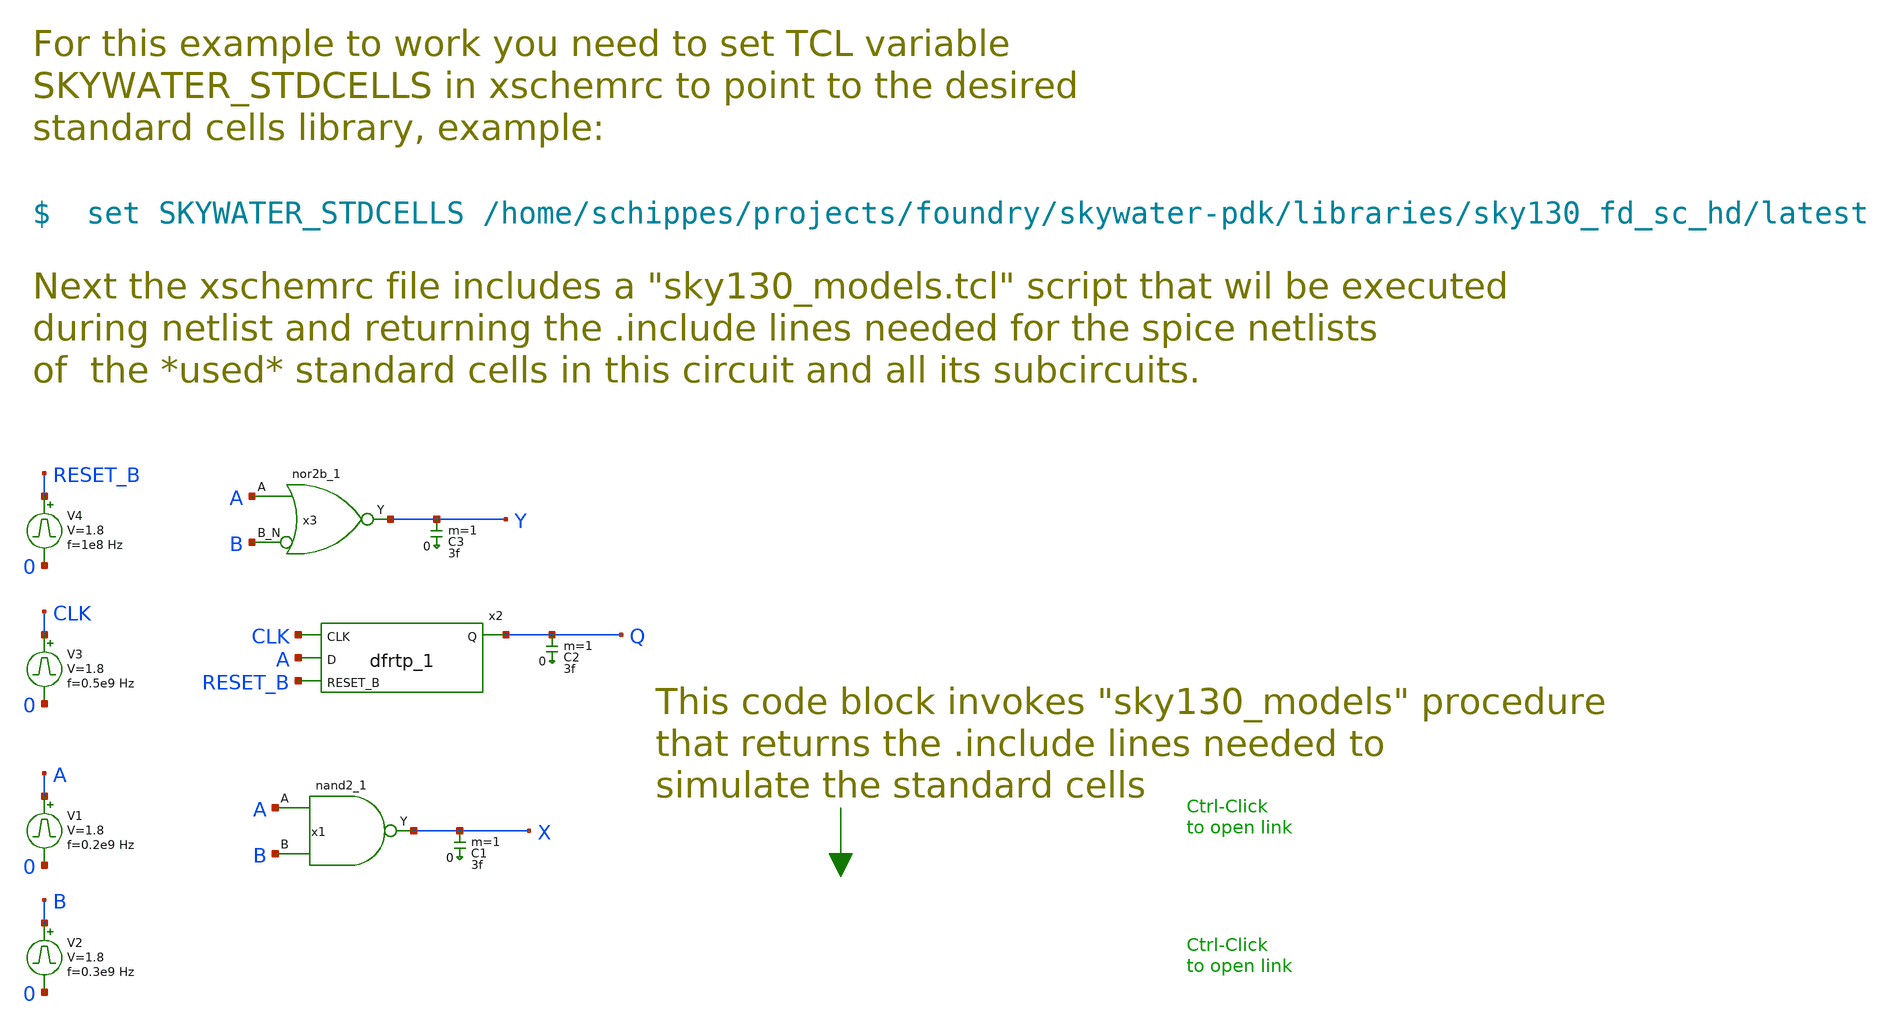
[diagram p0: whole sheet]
** sch_path: sky130_tests_X/test_stdcells.sch
* Copyright 2020 Stefan Frederik Schippers
* Licensed under the Apache License, Version 2.0 (the "License");
* you may not use this file except in compliance with the License.
* You may obtain a copy of the License at
* https://www.apache.org/licenses/LICENSE-2.0
* Unless required by applicable law or agreed to in writing, software
* distributed under the License is distributed on an "AS IS" BASIS,
* WITHOUT WARRANTIES OR CONDITIONS OF ANY KIND, either express or implied.
* See the License for the specific language governing permissions and
* limitations under the License.
**.subckt test_stdcells
x1 A B VSS VSS VCC VCC X sky130_fd_sc_hd__nand2_1
V1 A 0 pulse 0 1.8 '0.495/ 0.2e9 ' '0.01/0.2e9 ' '0.01/0.2e9 ' '0.49/0.2e9 ' '1/0.2e9 '
V2 B 0 pulse 0 1.8 '0.495/ 0.3e9 ' '0.01/0.3e9 ' '0.01/0.3e9 ' '0.49/0.3e9 ' '1/0.3e9 '
C1 X 0 3f m=1
x2 CLK A RESET_B VSS VSS VCC VCC Q sky130_fd_sc_hd__dfrtp_1
V3 CLK 0 pulse 0 1.8 '0.495/ 0.5e9 ' '0.01/0.5e9 ' '0.01/0.5e9 ' '0.49/0.5e9 ' '1/0.5e9 '
V4 RESET_B 0 pulse 0 1.8 '0.495/ 1e8 ' '0.01/1e8 ' '0.01/1e8 ' '0.49/1e8 ' '1/1e8 '
C2 Q 0 3f m=1
C3 Y 0 3f m=1
x3 A B VSS VSS VCC VCC Y sky130_fd_sc_hd__nor2b_1
**** begin user architecture code


.temp 25
vvcc vcc 0 dc 1.8
vvss vss 0 0
.control
tran 30p 80n
plot a b+2 clk+4 reset_b+6 x+8 y+10 q+12
.endc



**** end user architecture code
**.ends
**** begin user architecture code
 [sky130_models]
**** end user architecture code
.end
